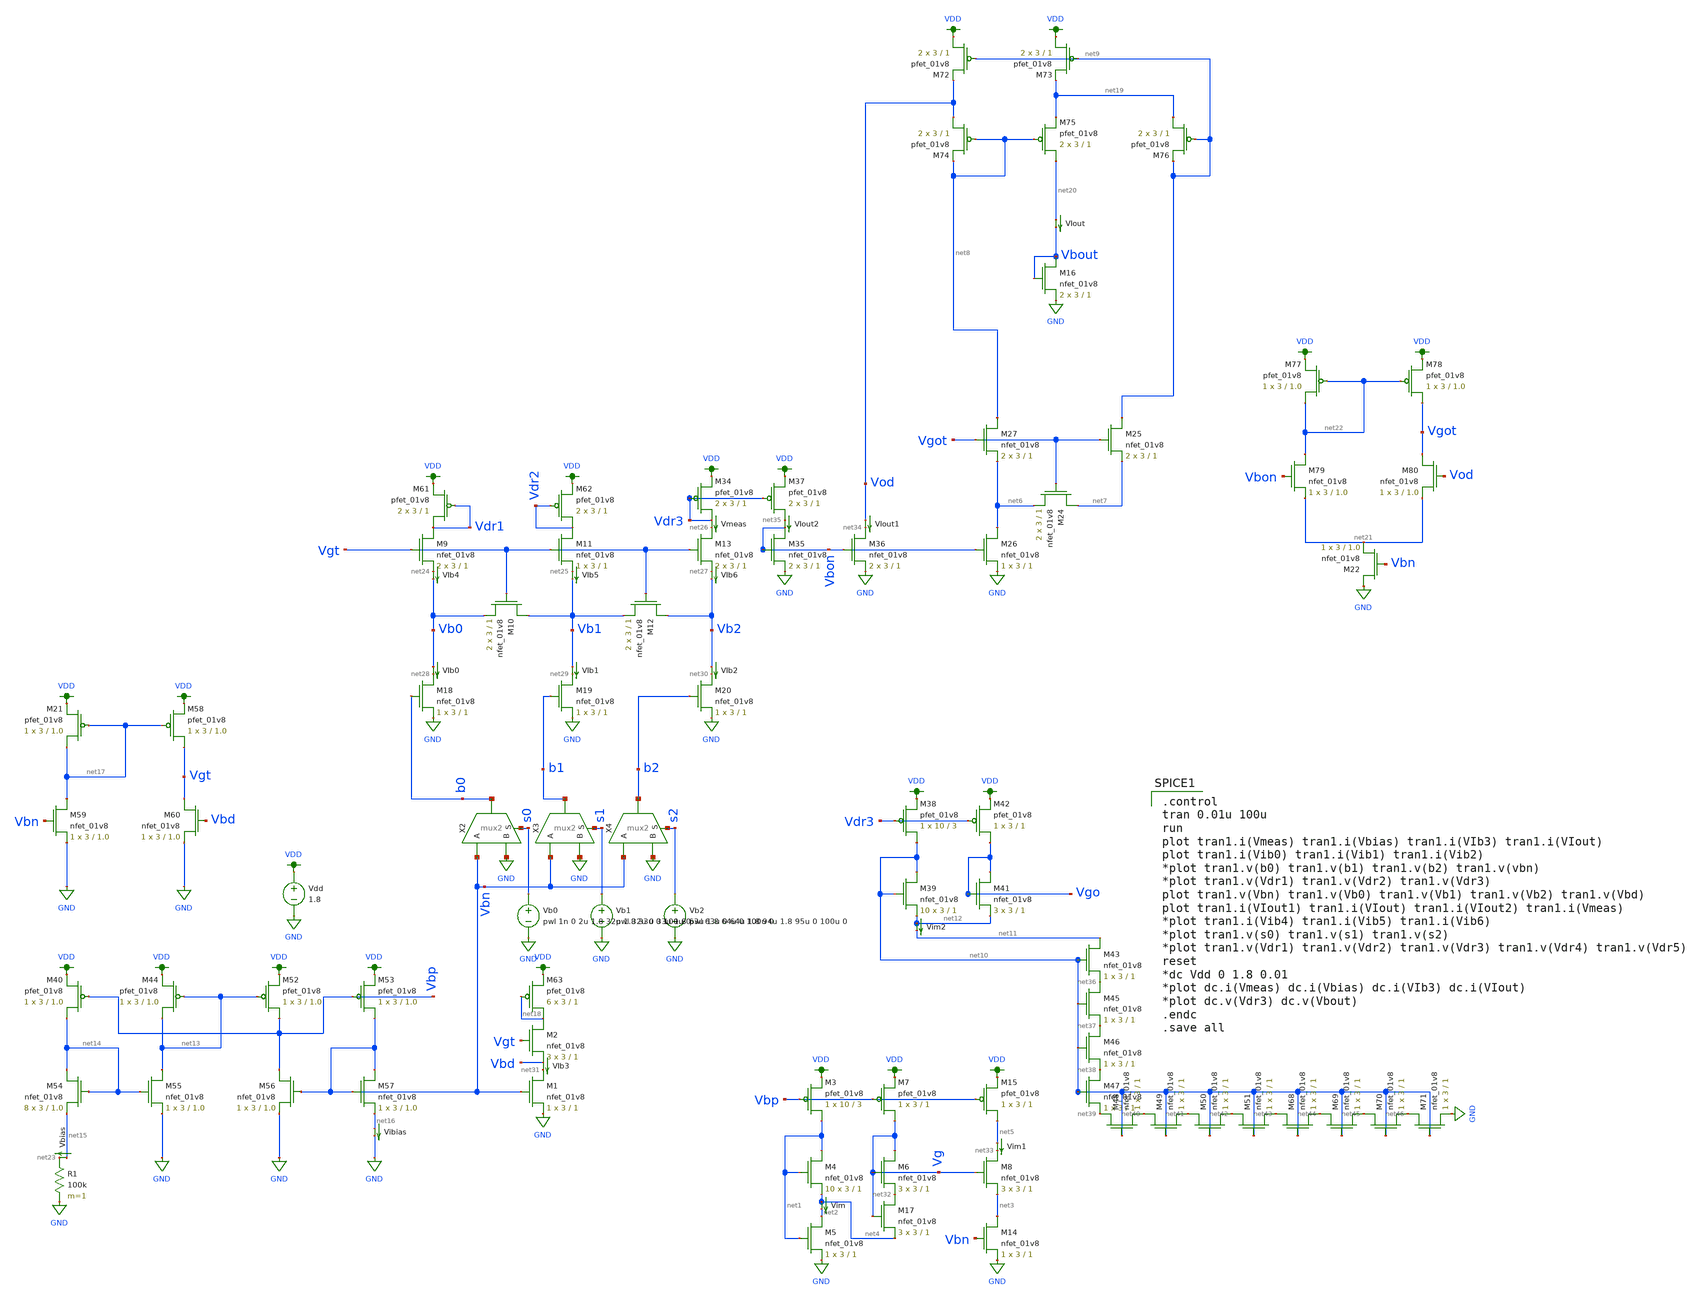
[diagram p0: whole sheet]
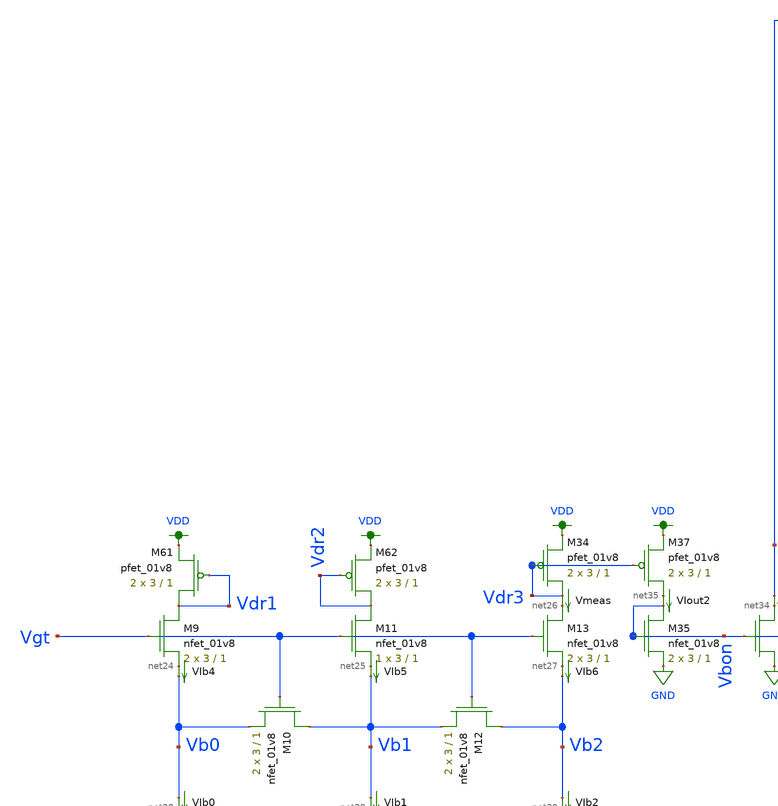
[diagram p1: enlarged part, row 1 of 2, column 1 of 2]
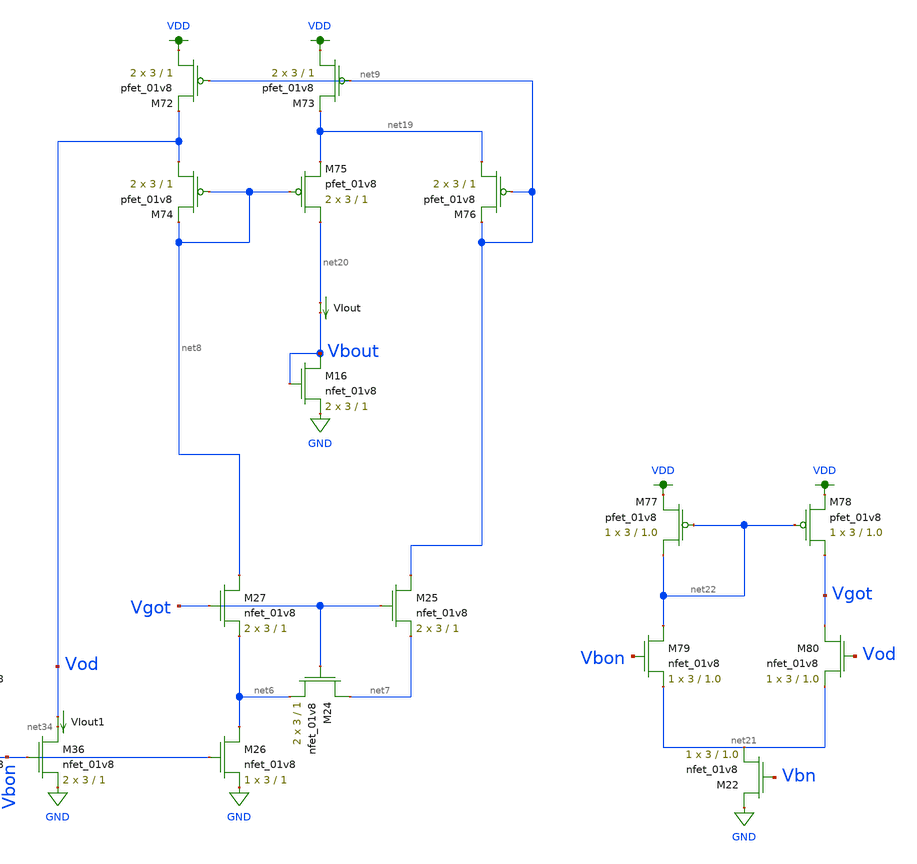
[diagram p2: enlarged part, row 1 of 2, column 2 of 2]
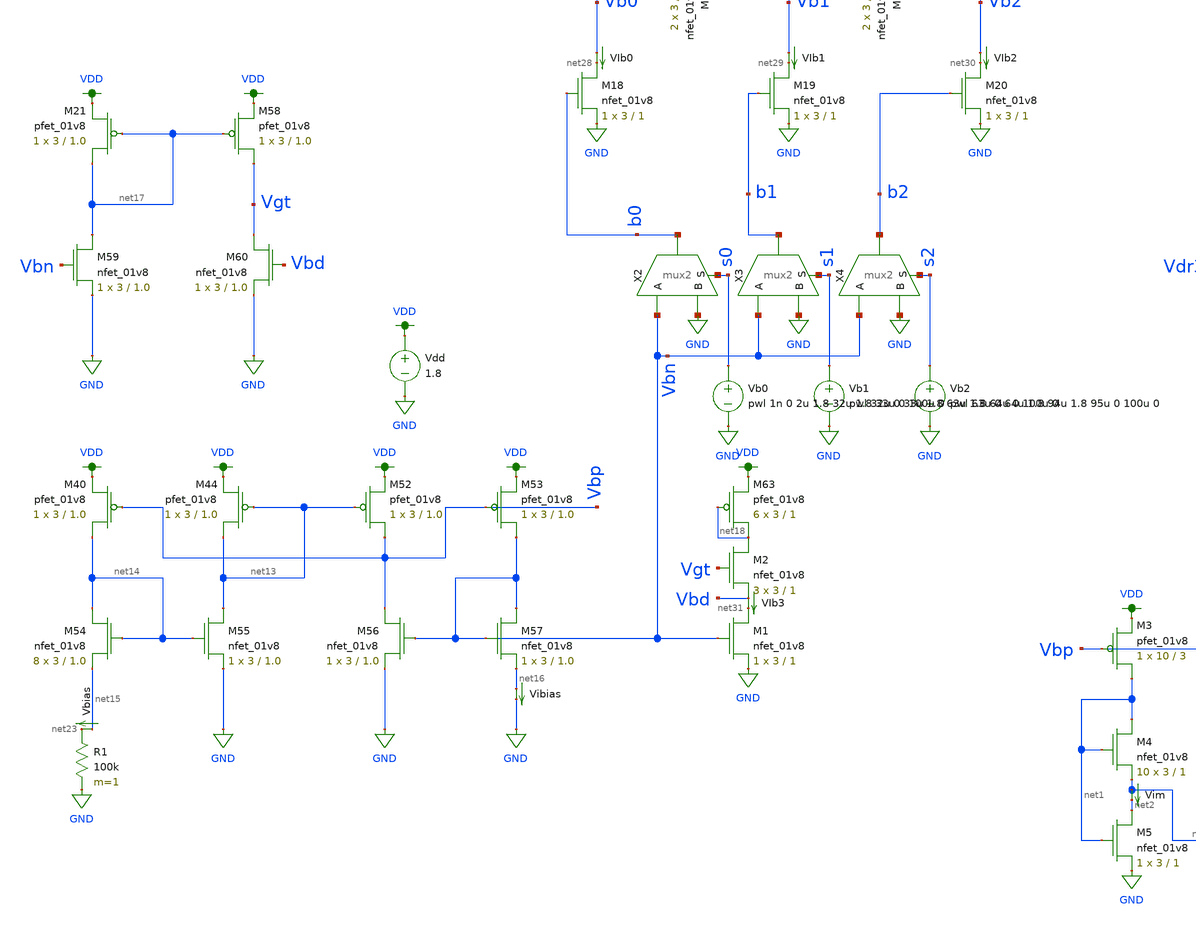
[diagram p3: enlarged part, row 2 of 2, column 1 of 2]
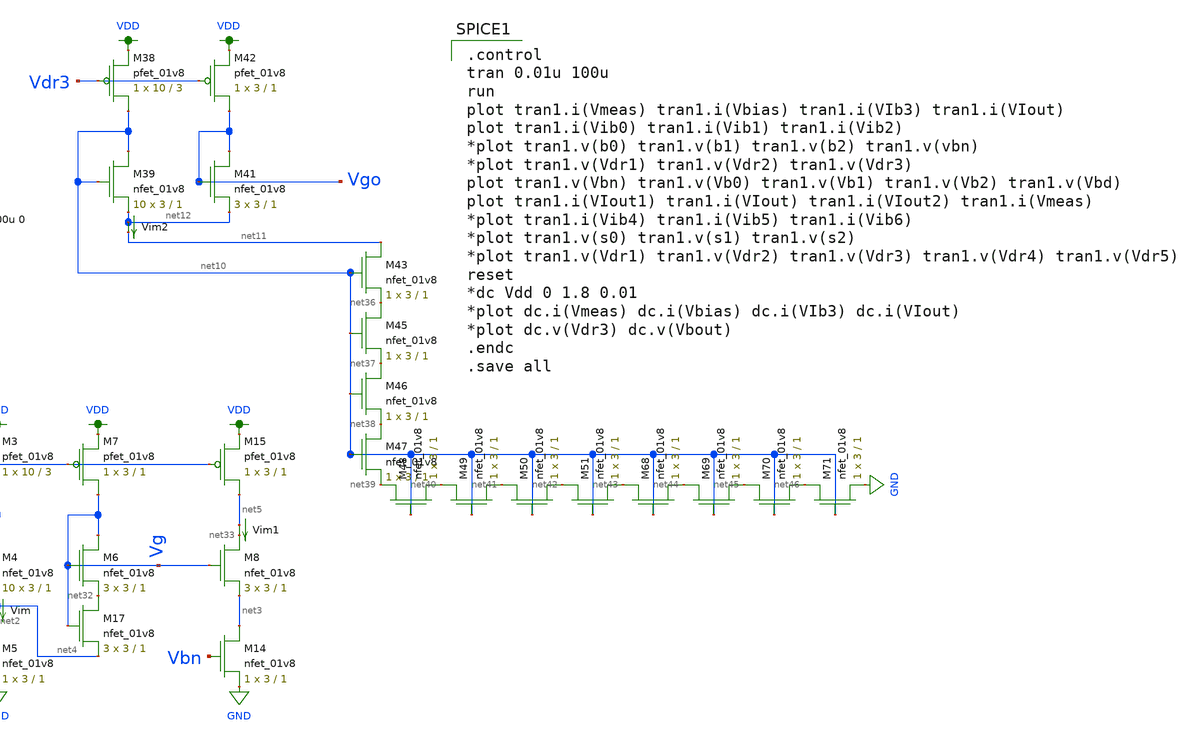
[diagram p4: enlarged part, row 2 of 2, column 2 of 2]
** sch_path: schematic/ladder3_test_josh_wilson_dynamic.sch
**.subckt ladder3_test_josh_wilson_dynamic
X2 b0 Vbn GND s0 mux2
X3 b1 Vbn GND s1 mux2
X4 b2 Vbn GND s2 mux2
R1 net23 GND 100k m=1
Vdd VDD GND 1.8
Vb0 s0 GND pwl 1n 0 2u 1.8 32u 1.8 33u 0 100u 0
Vb1 s1 GND pwl 32u 0 33u 1.8 63u 1.8 64u 0 100u 0
Vb2 s2 GND pwl 63u 0 64u 1.8 94u 1.8 95u 0 100u 0
XM9 Vdr1 Vgt net24 GND sky130_fd_pr__nfet_01v8 L=1 W=3 nf=1 ad='int((nf+1)/2) * W/nf * 0.29' as='int((nf+2)/2) * W/nf * 0.29'
+ pd='2*int((nf+1)/2) * (W/nf + 0.29)' ps='2*int((nf+2)/2) * (W/nf + 0.29)' nrd='0.29 / W' nrs='0.29 / W'
+ sa=0 sb=0 sd=0 mult=2 m=2
XM10 Vb1 Vgt Vb0 GND sky130_fd_pr__nfet_01v8 L=1 W=3 nf=1 ad='int((nf+1)/2) * W/nf * 0.29' as='int((nf+2)/2) * W/nf * 0.29'
+ pd='2*int((nf+1)/2) * (W/nf + 0.29)' ps='2*int((nf+2)/2) * (W/nf + 0.29)' nrd='0.29 / W' nrs='0.29 / W'
+ sa=0 sb=0 sd=0 mult=2 m=2
XM11 Vdr2 Vgt net25 GND sky130_fd_pr__nfet_01v8 L=1 W=3 nf=1 ad='int((nf+1)/2) * W/nf * 0.29' as='int((nf+2)/2) * W/nf * 0.29'
+ pd='2*int((nf+1)/2) * (W/nf + 0.29)' ps='2*int((nf+2)/2) * (W/nf + 0.29)' nrd='0.29 / W' nrs='0.29 / W'
+ sa=0 sb=0 sd=0 mult=1 m=1
XM12 Vb2 Vgt Vb1 GND sky130_fd_pr__nfet_01v8 L=1 W=3 nf=1 ad='int((nf+1)/2) * W/nf * 0.29' as='int((nf+2)/2) * W/nf * 0.29'
+ pd='2*int((nf+1)/2) * (W/nf + 0.29)' ps='2*int((nf+2)/2) * (W/nf + 0.29)' nrd='0.29 / W' nrs='0.29 / W'
+ sa=0 sb=0 sd=0 mult=2 m=2
XM13 net26 Vgt net27 GND sky130_fd_pr__nfet_01v8 L=1 W=3 nf=1 ad='int((nf+1)/2) * W/nf * 0.29' as='int((nf+2)/2) * W/nf * 0.29'
+ pd='2*int((nf+1)/2) * (W/nf + 0.29)' ps='2*int((nf+2)/2) * (W/nf + 0.29)' nrd='0.29 / W' nrs='0.29 / W'
+ sa=0 sb=0 sd=0 mult=2 m=2
XM18 net28 b0 GND GND sky130_fd_pr__nfet_01v8 L=1 W=3 nf=1 ad='int((nf+1)/2) * W/nf * 0.29' as='int((nf+2)/2) * W/nf * 0.29'
+ pd='2*int((nf+1)/2) * (W/nf + 0.29)' ps='2*int((nf+2)/2) * (W/nf + 0.29)' nrd='0.29 / W' nrs='0.29 / W'
+ sa=0 sb=0 sd=0 mult=1 m=1
XM19 net29 b1 GND GND sky130_fd_pr__nfet_01v8 L=1 W=3 nf=1 ad='int((nf+1)/2) * W/nf * 0.29' as='int((nf+2)/2) * W/nf * 0.29'
+ pd='2*int((nf+1)/2) * (W/nf + 0.29)' ps='2*int((nf+2)/2) * (W/nf + 0.29)' nrd='0.29 / W' nrs='0.29 / W'
+ sa=0 sb=0 sd=0 mult=1 m=1
XM20 net30 b2 GND GND sky130_fd_pr__nfet_01v8 L=1 W=3 nf=1 ad='int((nf+1)/2) * W/nf * 0.29' as='int((nf+2)/2) * W/nf * 0.29'
+ pd='2*int((nf+1)/2) * (W/nf + 0.29)' ps='2*int((nf+2)/2) * (W/nf + 0.29)' nrd='0.29 / W' nrs='0.29 / W'
+ sa=0 sb=0 sd=0 mult=1 m=1
Vmeas Vdr3 net26 0
.save i(vmeas)
Vbias net15 net23 0
.save i(vbias)
VIb0 Vb0 net28 0
.save i(vib0)
VIb1 Vb1 net29 0
.save i(vib1)
VIb2 Vb2 net30 0
.save i(vib2)
XM1 net31 Vbn GND GND sky130_fd_pr__nfet_01v8 L=1 W=3 nf=1 ad='int((nf+1)/2) * W/nf * 0.29' as='int((nf+2)/2) * W/nf * 0.29'
+ pd='2*int((nf+1)/2) * (W/nf + 0.29)' ps='2*int((nf+2)/2) * (W/nf + 0.29)' nrd='0.29 / W' nrs='0.29 / W'
+ sa=0 sb=0 sd=0 mult=1 m=1
VIb3 Vbd net31 0
.save i(vib3)
XM3 net1 Vbp VDD VDD sky130_fd_pr__pfet_01v8 L=3 W=10 nf=1 ad='int((nf+1)/2) * W/nf * 0.29' as='int((nf+2)/2) * W/nf * 0.29'
+ pd='2*int((nf+1)/2) * (W/nf + 0.29)' ps='2*int((nf+2)/2) * (W/nf + 0.29)' nrd='0.29 / W' nrs='0.29 / W'
+ sa=0 sb=0 sd=0 mult=1 m=1
XM4 net1 net1 net4 GND sky130_fd_pr__nfet_01v8 L=1 W=3 nf=1 ad='int((nf+1)/2) * W/nf * 0.29' as='int((nf+2)/2) * W/nf * 0.29'
+ pd='2*int((nf+1)/2) * (W/nf + 0.29)' ps='2*int((nf+2)/2) * (W/nf + 0.29)' nrd='0.29 / W' nrs='0.29 / W'
+ sa=0 sb=0 sd=0 mult=10 m=10
XM5 net2 net1 GND GND sky130_fd_pr__nfet_01v8 L=1 W=3 nf=1 ad='int((nf+1)/2) * W/nf * 0.29' as='int((nf+2)/2) * W/nf * 0.29'
+ pd='2*int((nf+1)/2) * (W/nf + 0.29)' ps='2*int((nf+2)/2) * (W/nf + 0.29)' nrd='0.29 / W' nrs='0.29 / W'
+ sa=0 sb=0 sd=0 mult=1 m=1
Vim net4 net2 0
.save i(vim)
XM6 Vg Vg net32 GND sky130_fd_pr__nfet_01v8 L=1 W=3 nf=1 ad='int((nf+1)/2) * W/nf * 0.29' as='int((nf+2)/2) * W/nf * 0.29'
+ pd='2*int((nf+1)/2) * (W/nf + 0.29)' ps='2*int((nf+2)/2) * (W/nf + 0.29)' nrd='0.29 / W' nrs='0.29 / W'
+ sa=0 sb=0 sd=0 mult=3 m=3
XM7 Vg Vbp VDD VDD sky130_fd_pr__pfet_01v8 L=1 W=3 nf=1 ad='int((nf+1)/2) * W/nf * 0.29' as='int((nf+2)/2) * W/nf * 0.29'
+ pd='2*int((nf+1)/2) * (W/nf + 0.29)' ps='2*int((nf+2)/2) * (W/nf + 0.29)' nrd='0.29 / W' nrs='0.29 / W'
+ sa=0 sb=0 sd=0 mult=1 m=1
XM8 net33 Vg net3 GND sky130_fd_pr__nfet_01v8 L=1 W=3 nf=1 ad='int((nf+1)/2) * W/nf * 0.29' as='int((nf+2)/2) * W/nf * 0.29'
+ pd='2*int((nf+1)/2) * (W/nf + 0.29)' ps='2*int((nf+2)/2) * (W/nf + 0.29)' nrd='0.29 / W' nrs='0.29 / W'
+ sa=0 sb=0 sd=0 mult=3 m=3
XM14 net3 Vbn GND GND sky130_fd_pr__nfet_01v8 L=1 W=3 nf=1 ad='int((nf+1)/2) * W/nf * 0.29' as='int((nf+2)/2) * W/nf * 0.29'
+ pd='2*int((nf+1)/2) * (W/nf + 0.29)' ps='2*int((nf+2)/2) * (W/nf + 0.29)' nrd='0.29 / W' nrs='0.29 / W'
+ sa=0 sb=0 sd=0 mult=1 m=1
Vim1 net5 net33 0
.save i(vim1)
XM15 net5 Vbp VDD VDD sky130_fd_pr__pfet_01v8 L=1 W=3 nf=1 ad='int((nf+1)/2) * W/nf * 0.29' as='int((nf+2)/2) * W/nf * 0.29'
+ pd='2*int((nf+1)/2) * (W/nf + 0.29)' ps='2*int((nf+2)/2) * (W/nf + 0.29)' nrd='0.29 / W' nrs='0.29 / W'
+ sa=0 sb=0 sd=0 mult=1 m=1
VIb4 net24 Vb0 0
.save i(vib4)
VIb5 net25 Vb1 0
.save i(vib5)
VIb6 net27 Vb2 0
.save i(vib6)
VIout net20 Vbout 0
.save i(viout)
XM24 net7 Vgot net6 GND sky130_fd_pr__nfet_01v8 L=1 W=3 nf=1 ad='int((nf+1)/2) * W/nf * 0.29' as='int((nf+2)/2) * W/nf * 0.29'
+ pd='2*int((nf+1)/2) * (W/nf + 0.29)' ps='2*int((nf+2)/2) * (W/nf + 0.29)' nrd='0.29 / W' nrs='0.29 / W'
+ sa=0 sb=0 sd=0 mult=2 m=2
XM25 net9 Vgot net7 GND sky130_fd_pr__nfet_01v8 L=1 W=3 nf=1 ad='int((nf+1)/2) * W/nf * 0.29' as='int((nf+2)/2) * W/nf * 0.29'
+ pd='2*int((nf+1)/2) * (W/nf + 0.29)' ps='2*int((nf+2)/2) * (W/nf + 0.29)' nrd='0.29 / W' nrs='0.29 / W'
+ sa=0 sb=0 sd=0 mult=2 m=2
XM26 net6 Vbon GND GND sky130_fd_pr__nfet_01v8 L=1 W=3 nf=1 ad='int((nf+1)/2) * W/nf * 0.29' as='int((nf+2)/2) * W/nf * 0.29'
+ pd='2*int((nf+1)/2) * (W/nf + 0.29)' ps='2*int((nf+2)/2) * (W/nf + 0.29)' nrd='0.29 / W' nrs='0.29 / W'
+ sa=0 sb=0 sd=0 mult=1 m=1
XM27 net8 Vgot net6 GND sky130_fd_pr__nfet_01v8 L=1 W=3 nf=1 ad='int((nf+1)/2) * W/nf * 0.29' as='int((nf+2)/2) * W/nf * 0.29'
+ pd='2*int((nf+1)/2) * (W/nf + 0.29)' ps='2*int((nf+2)/2) * (W/nf + 0.29)' nrd='0.29 / W' nrs='0.29 / W'
+ sa=0 sb=0 sd=0 mult=2 m=2
XM16 Vbout Vbout GND GND sky130_fd_pr__nfet_01v8 L=1 W=3 nf=1 ad='int((nf+1)/2) * W/nf * 0.29' as='int((nf+2)/2) * W/nf * 0.29'
+ pd='2*int((nf+1)/2) * (W/nf + 0.29)' ps='2*int((nf+2)/2) * (W/nf + 0.29)' nrd='0.29 / W' nrs='0.29 / W'
+ sa=0 sb=0 sd=0 mult=2 m=2
XM34 Vdr3 Vdr3 VDD VDD sky130_fd_pr__pfet_01v8 L=1 W=3 nf=1 ad='int((nf+1)/2) * W/nf * 0.29' as='int((nf+2)/2) * W/nf * 0.29'
+ pd='2*int((nf+1)/2) * (W/nf + 0.29)' ps='2*int((nf+2)/2) * (W/nf + 0.29)' nrd='0.29 / W' nrs='0.29 / W'
+ sa=0 sb=0 sd=0 mult=2 m=2
XM35 Vbon Vbon GND GND sky130_fd_pr__nfet_01v8 L=1 W=3 nf=1 ad='int((nf+1)/2) * W/nf * 0.29' as='int((nf+2)/2) * W/nf * 0.29'
+ pd='2*int((nf+1)/2) * (W/nf + 0.29)' ps='2*int((nf+2)/2) * (W/nf + 0.29)' nrd='0.29 / W' nrs='0.29 / W'
+ sa=0 sb=0 sd=0 mult=2 m=2
XM36 net34 Vbon GND GND sky130_fd_pr__nfet_01v8 L=1 W=3 nf=1 ad='int((nf+1)/2) * W/nf * 0.29' as='int((nf+2)/2) * W/nf * 0.29'
+ pd='2*int((nf+1)/2) * (W/nf + 0.29)' ps='2*int((nf+2)/2) * (W/nf + 0.29)' nrd='0.29 / W' nrs='0.29 / W'
+ sa=0 sb=0 sd=0 mult=2 m=2
XM37 net35 Vdr3 VDD VDD sky130_fd_pr__pfet_01v8 L=1 W=3 nf=1 ad='int((nf+1)/2) * W/nf * 0.29' as='int((nf+2)/2) * W/nf * 0.29'
+ pd='2*int((nf+1)/2) * (W/nf + 0.29)' ps='2*int((nf+2)/2) * (W/nf + 0.29)' nrd='0.29 / W' nrs='0.29 / W'
+ sa=0 sb=0 sd=0 mult=2 m=2
XM38 net10 Vdr3 VDD VDD sky130_fd_pr__pfet_01v8 L=3 W=10 nf=1 ad='int((nf+1)/2) * W/nf * 0.29' as='int((nf+2)/2) * W/nf * 0.29'
+ pd='2*int((nf+1)/2) * (W/nf + 0.29)' ps='2*int((nf+2)/2) * (W/nf + 0.29)' nrd='0.29 / W' nrs='0.29 / W'
+ sa=0 sb=0 sd=0 mult=1 m=1
XM39 net10 net10 net12 GND sky130_fd_pr__nfet_01v8 L=1 W=3 nf=1 ad='int((nf+1)/2) * W/nf * 0.29' as='int((nf+2)/2) * W/nf * 0.29'
+ pd='2*int((nf+1)/2) * (W/nf + 0.29)' ps='2*int((nf+2)/2) * (W/nf + 0.29)' nrd='0.29 / W' nrs='0.29 / W'
+ sa=0 sb=0 sd=0 mult=10 m=10
Vim2 net12 net11 0
.save i(vim2)
XM41 Vgo Vgo net12 GND sky130_fd_pr__nfet_01v8 L=1 W=3 nf=1 ad='int((nf+1)/2) * W/nf * 0.29' as='int((nf+2)/2) * W/nf * 0.29'
+ pd='2*int((nf+1)/2) * (W/nf + 0.29)' ps='2*int((nf+2)/2) * (W/nf + 0.29)' nrd='0.29 / W' nrs='0.29 / W'
+ sa=0 sb=0 sd=0 mult=3 m=3
XM42 Vgo Vdr3 VDD VDD sky130_fd_pr__pfet_01v8 L=1 W=3 nf=1 ad='int((nf+1)/2) * W/nf * 0.29' as='int((nf+2)/2) * W/nf * 0.29'
+ pd='2*int((nf+1)/2) * (W/nf + 0.29)' ps='2*int((nf+2)/2) * (W/nf + 0.29)' nrd='0.29 / W' nrs='0.29 / W'
+ sa=0 sb=0 sd=0 mult=1 m=1
XM43 net11 net10 net36 GND sky130_fd_pr__nfet_01v8 L=1 W=3 nf=1 ad='int((nf+1)/2) * W/nf * 0.29' as='int((nf+2)/2) * W/nf * 0.29'
+ pd='2*int((nf+1)/2) * (W/nf + 0.29)' ps='2*int((nf+2)/2) * (W/nf + 0.29)' nrd='0.29 / W' nrs='0.29 / W'
+ sa=0 sb=0 sd=0 mult=1 m=1
XM45 net36 net10 net37 GND sky130_fd_pr__nfet_01v8 L=1 W=3 nf=1 ad='int((nf+1)/2) * W/nf * 0.29' as='int((nf+2)/2) * W/nf * 0.29'
+ pd='2*int((nf+1)/2) * (W/nf + 0.29)' ps='2*int((nf+2)/2) * (W/nf + 0.29)' nrd='0.29 / W' nrs='0.29 / W'
+ sa=0 sb=0 sd=0 mult=1 m=1
XM46 net37 net10 net38 GND sky130_fd_pr__nfet_01v8 L=1 W=3 nf=1 ad='int((nf+1)/2) * W/nf * 0.29' as='int((nf+2)/2) * W/nf * 0.29'
+ pd='2*int((nf+1)/2) * (W/nf + 0.29)' ps='2*int((nf+2)/2) * (W/nf + 0.29)' nrd='0.29 / W' nrs='0.29 / W'
+ sa=0 sb=0 sd=0 mult=1 m=1
XM47 net38 net10 net39 GND sky130_fd_pr__nfet_01v8 L=1 W=3 nf=1 ad='int((nf+1)/2) * W/nf * 0.29' as='int((nf+2)/2) * W/nf * 0.29'
+ pd='2*int((nf+1)/2) * (W/nf + 0.29)' ps='2*int((nf+2)/2) * (W/nf + 0.29)' nrd='0.29 / W' nrs='0.29 / W'
+ sa=0 sb=0 sd=0 mult=1 m=1
XM48 net39 net10 net40 GND sky130_fd_pr__nfet_01v8 L=1 W=3 nf=1 ad='int((nf+1)/2) * W/nf * 0.29' as='int((nf+2)/2) * W/nf * 0.29'
+ pd='2*int((nf+1)/2) * (W/nf + 0.29)' ps='2*int((nf+2)/2) * (W/nf + 0.29)' nrd='0.29 / W' nrs='0.29 / W'
+ sa=0 sb=0 sd=0 mult=1 m=1
XM49 net40 net10 net41 GND sky130_fd_pr__nfet_01v8 L=1 W=3 nf=1 ad='int((nf+1)/2) * W/nf * 0.29' as='int((nf+2)/2) * W/nf * 0.29'
+ pd='2*int((nf+1)/2) * (W/nf + 0.29)' ps='2*int((nf+2)/2) * (W/nf + 0.29)' nrd='0.29 / W' nrs='0.29 / W'
+ sa=0 sb=0 sd=0 mult=1 m=1
XM50 net41 net10 net42 GND sky130_fd_pr__nfet_01v8 L=1 W=3 nf=1 ad='int((nf+1)/2) * W/nf * 0.29' as='int((nf+2)/2) * W/nf * 0.29'
+ pd='2*int((nf+1)/2) * (W/nf + 0.29)' ps='2*int((nf+2)/2) * (W/nf + 0.29)' nrd='0.29 / W' nrs='0.29 / W'
+ sa=0 sb=0 sd=0 mult=1 m=1
XM51 net42 net10 net43 GND sky130_fd_pr__nfet_01v8 L=1 W=3 nf=1 ad='int((nf+1)/2) * W/nf * 0.29' as='int((nf+2)/2) * W/nf * 0.29'
+ pd='2*int((nf+1)/2) * (W/nf + 0.29)' ps='2*int((nf+2)/2) * (W/nf + 0.29)' nrd='0.29 / W' nrs='0.29 / W'
+ sa=0 sb=0 sd=0 mult=1 m=1
XM40 net14 Vbp VDD VDD sky130_fd_pr__pfet_01v8 L=1.0 W=3 nf=1 ad='int((nf+1)/2) * W/nf * 0.29' as='int((nf+2)/2) * W/nf * 0.29'
+ pd='2*int((nf+1)/2) * (W/nf + 0.29)' ps='2*int((nf+2)/2) * (W/nf + 0.29)' nrd='0.29 / W' nrs='0.29 / W'
+ sa=0 sb=0 sd=0 mult=1 m=1
XM44 net13 net13 VDD VDD sky130_fd_pr__pfet_01v8 L=1.0 W=3 nf=1 ad='int((nf+1)/2) * W/nf * 0.29' as='int((nf+2)/2) * W/nf * 0.29'
+ pd='2*int((nf+1)/2) * (W/nf + 0.29)' ps='2*int((nf+2)/2) * (W/nf + 0.29)' nrd='0.29 / W' nrs='0.29 / W'
+ sa=0 sb=0 sd=0 mult=1 m=1
XM52 Vbp net13 VDD VDD sky130_fd_pr__pfet_01v8 L=1.0 W=3 nf=1 ad='int((nf+1)/2) * W/nf * 0.29' as='int((nf+2)/2) * W/nf * 0.29'
+ pd='2*int((nf+1)/2) * (W/nf + 0.29)' ps='2*int((nf+2)/2) * (W/nf + 0.29)' nrd='0.29 / W' nrs='0.29 / W'
+ sa=0 sb=0 sd=0 mult=1 m=1
XM53 Vbn Vbp VDD VDD sky130_fd_pr__pfet_01v8 L=1.0 W=3 nf=1 ad='int((nf+1)/2) * W/nf * 0.29' as='int((nf+2)/2) * W/nf * 0.29'
+ pd='2*int((nf+1)/2) * (W/nf + 0.29)' ps='2*int((nf+2)/2) * (W/nf + 0.29)' nrd='0.29 / W' nrs='0.29 / W'
+ sa=0 sb=0 sd=0 mult=1 m=1
XM54 net14 net14 net15 GND sky130_fd_pr__nfet_01v8 L=1.0 W=3 nf=1 ad='int((nf+1)/2) * W/nf * 0.29' as='int((nf+2)/2) * W/nf * 0.29'
+ pd='2*int((nf+1)/2) * (W/nf + 0.29)' ps='2*int((nf+2)/2) * (W/nf + 0.29)' nrd='0.29 / W' nrs='0.29 / W'
+ sa=0 sb=0 sd=0 mult=8 m=8
XM55 net13 net14 GND GND sky130_fd_pr__nfet_01v8 L=1.0 W=3 nf=1 ad='int((nf+1)/2) * W/nf * 0.29' as='int((nf+2)/2) * W/nf * 0.29'
+ pd='2*int((nf+1)/2) * (W/nf + 0.29)' ps='2*int((nf+2)/2) * (W/nf + 0.29)' nrd='0.29 / W' nrs='0.29 / W'
+ sa=0 sb=0 sd=0 mult=1 m=1
XM56 Vbp Vbn GND GND sky130_fd_pr__nfet_01v8 L=1.0 W=3 nf=1 ad='int((nf+1)/2) * W/nf * 0.29' as='int((nf+2)/2) * W/nf * 0.29'
+ pd='2*int((nf+1)/2) * (W/nf + 0.29)' ps='2*int((nf+2)/2) * (W/nf + 0.29)' nrd='0.29 / W' nrs='0.29 / W'
+ sa=0 sb=0 sd=0 mult=1 m=1
XM57 Vbn Vbn net16 GND sky130_fd_pr__nfet_01v8 L=1.0 W=3 nf=1 ad='int((nf+1)/2) * W/nf * 0.29' as='int((nf+2)/2) * W/nf * 0.29'
+ pd='2*int((nf+1)/2) * (W/nf + 0.29)' ps='2*int((nf+2)/2) * (W/nf + 0.29)' nrd='0.29 / W' nrs='0.29 / W'
+ sa=0 sb=0 sd=0 mult=1 m=1
Vibias net16 GND 0
.save i(vibias)
XM2 net18 Vgt Vbd GND sky130_fd_pr__nfet_01v8 L=1 W=3 nf=1 ad='int((nf+1)/2) * W/nf * 0.29' as='int((nf+2)/2) * W/nf * 0.29'
+ pd='2*int((nf+1)/2) * (W/nf + 0.29)' ps='2*int((nf+2)/2) * (W/nf + 0.29)' nrd='0.29 / W' nrs='0.29 / W'
+ sa=0 sb=0 sd=0 mult=3 m=3
XM17 net32 Vg net4 GND sky130_fd_pr__nfet_01v8 L=1 W=3 nf=1 ad='int((nf+1)/2) * W/nf * 0.29' as='int((nf+2)/2) * W/nf * 0.29'
+ pd='2*int((nf+1)/2) * (W/nf + 0.29)' ps='2*int((nf+2)/2) * (W/nf + 0.29)' nrd='0.29 / W' nrs='0.29 / W'
+ sa=0 sb=0 sd=0 mult=3 m=3
XM21 net17 net17 VDD VDD sky130_fd_pr__pfet_01v8 L=1.0 W=3 nf=1 ad='int((nf+1)/2) * W/nf * 0.29' as='int((nf+2)/2) * W/nf * 0.29'
+ pd='2*int((nf+1)/2) * (W/nf + 0.29)' ps='2*int((nf+2)/2) * (W/nf + 0.29)' nrd='0.29 / W' nrs='0.29 / W'
+ sa=0 sb=0 sd=0 mult=1 m=1
XM58 Vgt net17 VDD VDD sky130_fd_pr__pfet_01v8 L=1.0 W=3 nf=1 ad='int((nf+1)/2) * W/nf * 0.29' as='int((nf+2)/2) * W/nf * 0.29'
+ pd='2*int((nf+1)/2) * (W/nf + 0.29)' ps='2*int((nf+2)/2) * (W/nf + 0.29)' nrd='0.29 / W' nrs='0.29 / W'
+ sa=0 sb=0 sd=0 mult=1 m=1
XM59 net17 Vbn GND GND sky130_fd_pr__nfet_01v8 L=1.0 W=3 nf=1 ad='int((nf+1)/2) * W/nf * 0.29' as='int((nf+2)/2) * W/nf * 0.29'
+ pd='2*int((nf+1)/2) * (W/nf + 0.29)' ps='2*int((nf+2)/2) * (W/nf + 0.29)' nrd='0.29 / W' nrs='0.29 / W'
+ sa=0 sb=0 sd=0 mult=1 m=1
XM60 Vgt Vbd GND GND sky130_fd_pr__nfet_01v8 L=1.0 W=3 nf=1 ad='int((nf+1)/2) * W/nf * 0.29' as='int((nf+2)/2) * W/nf * 0.29'
+ pd='2*int((nf+1)/2) * (W/nf + 0.29)' ps='2*int((nf+2)/2) * (W/nf + 0.29)' nrd='0.29 / W' nrs='0.29 / W'
+ sa=0 sb=0 sd=0 mult=1 m=1
XM61 Vdr1 Vdr1 VDD VDD sky130_fd_pr__pfet_01v8 L=1 W=3 nf=1 ad='int((nf+1)/2) * W/nf * 0.29' as='int((nf+2)/2) * W/nf * 0.29'
+ pd='2*int((nf+1)/2) * (W/nf + 0.29)' ps='2*int((nf+2)/2) * (W/nf + 0.29)' nrd='0.29 / W' nrs='0.29 / W'
+ sa=0 sb=0 sd=0 mult=2 m=2
XM62 Vdr2 Vdr2 VDD VDD sky130_fd_pr__pfet_01v8 L=1 W=3 nf=1 ad='int((nf+1)/2) * W/nf * 0.29' as='int((nf+2)/2) * W/nf * 0.29'
+ pd='2*int((nf+1)/2) * (W/nf + 0.29)' ps='2*int((nf+2)/2) * (W/nf + 0.29)' nrd='0.29 / W' nrs='0.29 / W'
+ sa=0 sb=0 sd=0 mult=2 m=2
XM63 net18 net18 VDD VDD sky130_fd_pr__pfet_01v8 L=1 W=3 nf=1 ad='int((nf+1)/2) * W/nf * 0.29' as='int((nf+2)/2) * W/nf * 0.29'
+ pd='2*int((nf+1)/2) * (W/nf + 0.29)' ps='2*int((nf+2)/2) * (W/nf + 0.29)' nrd='0.29 / W' nrs='0.29 / W'
+ sa=0 sb=0 sd=0 mult=6 m=6
XM68 net43 net10 net44 GND sky130_fd_pr__nfet_01v8 L=1 W=3 nf=1 ad='int((nf+1)/2) * W/nf * 0.29' as='int((nf+2)/2) * W/nf * 0.29'
+ pd='2*int((nf+1)/2) * (W/nf + 0.29)' ps='2*int((nf+2)/2) * (W/nf + 0.29)' nrd='0.29 / W' nrs='0.29 / W'
+ sa=0 sb=0 sd=0 mult=1 m=1
XM69 net44 net10 net45 GND sky130_fd_pr__nfet_01v8 L=1 W=3 nf=1 ad='int((nf+1)/2) * W/nf * 0.29' as='int((nf+2)/2) * W/nf * 0.29'
+ pd='2*int((nf+1)/2) * (W/nf + 0.29)' ps='2*int((nf+2)/2) * (W/nf + 0.29)' nrd='0.29 / W' nrs='0.29 / W'
+ sa=0 sb=0 sd=0 mult=1 m=1
XM70 net45 net10 net46 GND sky130_fd_pr__nfet_01v8 L=1 W=3 nf=1 ad='int((nf+1)/2) * W/nf * 0.29' as='int((nf+2)/2) * W/nf * 0.29'
+ pd='2*int((nf+1)/2) * (W/nf + 0.29)' ps='2*int((nf+2)/2) * (W/nf + 0.29)' nrd='0.29 / W' nrs='0.29 / W'
+ sa=0 sb=0 sd=0 mult=1 m=1
XM71 net46 net10 GND GND sky130_fd_pr__nfet_01v8 L=1 W=3 nf=1 ad='int((nf+1)/2) * W/nf * 0.29' as='int((nf+2)/2) * W/nf * 0.29'
+ pd='2*int((nf+1)/2) * (W/nf + 0.29)' ps='2*int((nf+2)/2) * (W/nf + 0.29)' nrd='0.29 / W' nrs='0.29 / W'
+ sa=0 sb=0 sd=0 mult=1 m=1
VIout1 Vod net34 0
.save i(viout1)
VIout2 net35 Vbon 0
.save i(viout2)
XM72 VDD net9 Vod VDD sky130_fd_pr__pfet_01v8 L=1 W=3 nf=1 ad='int((nf+1)/2) * W/nf * 0.29' as='int((nf+2)/2) * W/nf * 0.29'
+ pd='2*int((nf+1)/2) * (W/nf + 0.29)' ps='2*int((nf+2)/2) * (W/nf + 0.29)' nrd='0.29 / W' nrs='0.29 / W'
+ sa=0 sb=0 sd=0 mult=2 m=2
XM73 VDD net9 net19 VDD sky130_fd_pr__pfet_01v8 L=1 W=3 nf=1 ad='int((nf+1)/2) * W/nf * 0.29' as='int((nf+2)/2) * W/nf * 0.29'
+ pd='2*int((nf+1)/2) * (W/nf + 0.29)' ps='2*int((nf+2)/2) * (W/nf + 0.29)' nrd='0.29 / W' nrs='0.29 / W'
+ sa=0 sb=0 sd=0 mult=2 m=2
XM74 Vod net8 net8 VDD sky130_fd_pr__pfet_01v8 L=1 W=3 nf=1 ad='int((nf+1)/2) * W/nf * 0.29' as='int((nf+2)/2) * W/nf * 0.29'
+ pd='2*int((nf+1)/2) * (W/nf + 0.29)' ps='2*int((nf+2)/2) * (W/nf + 0.29)' nrd='0.29 / W' nrs='0.29 / W'
+ sa=0 sb=0 sd=0 mult=2 m=2
XM75 net20 net8 net19 VDD sky130_fd_pr__pfet_01v8 L=1 W=3 nf=1 ad='int((nf+1)/2) * W/nf * 0.29' as='int((nf+2)/2) * W/nf * 0.29'
+ pd='2*int((nf+1)/2) * (W/nf + 0.29)' ps='2*int((nf+2)/2) * (W/nf + 0.29)' nrd='0.29 / W' nrs='0.29 / W'
+ sa=0 sb=0 sd=0 mult=2 m=2
XM76 net19 net9 net9 VDD sky130_fd_pr__pfet_01v8 L=1 W=3 nf=1 ad='int((nf+1)/2) * W/nf * 0.29' as='int((nf+2)/2) * W/nf * 0.29'
+ pd='2*int((nf+1)/2) * (W/nf + 0.29)' ps='2*int((nf+2)/2) * (W/nf + 0.29)' nrd='0.29 / W' nrs='0.29 / W'
+ sa=0 sb=0 sd=0 mult=2 m=2
XM77 net22 net22 VDD VDD sky130_fd_pr__pfet_01v8 L=1.0 W=3 nf=1 ad='int((nf+1)/2) * W/nf * 0.29' as='int((nf+2)/2) * W/nf * 0.29'
+ pd='2*int((nf+1)/2) * (W/nf + 0.29)' ps='2*int((nf+2)/2) * (W/nf + 0.29)' nrd='0.29 / W' nrs='0.29 / W'
+ sa=0 sb=0 sd=0 mult=1 m=1
XM78 Vgot net22 VDD VDD sky130_fd_pr__pfet_01v8 L=1.0 W=3 nf=1 ad='int((nf+1)/2) * W/nf * 0.29' as='int((nf+2)/2) * W/nf * 0.29'
+ pd='2*int((nf+1)/2) * (W/nf + 0.29)' ps='2*int((nf+2)/2) * (W/nf + 0.29)' nrd='0.29 / W' nrs='0.29 / W'
+ sa=0 sb=0 sd=0 mult=1 m=1
XM79 net22 Vbon net21 GND sky130_fd_pr__nfet_01v8 L=1.0 W=3 nf=1 ad='int((nf+1)/2) * W/nf * 0.29' as='int((nf+2)/2) * W/nf * 0.29'
+ pd='2*int((nf+1)/2) * (W/nf + 0.29)' ps='2*int((nf+2)/2) * (W/nf + 0.29)' nrd='0.29 / W' nrs='0.29 / W'
+ sa=0 sb=0 sd=0 mult=1 m=1
XM80 Vgot Vod net21 GND sky130_fd_pr__nfet_01v8 L=1.0 W=3 nf=1 ad='int((nf+1)/2) * W/nf * 0.29' as='int((nf+2)/2) * W/nf * 0.29'
+ pd='2*int((nf+1)/2) * (W/nf + 0.29)' ps='2*int((nf+2)/2) * (W/nf + 0.29)' nrd='0.29 / W' nrs='0.29 / W'
+ sa=0 sb=0 sd=0 mult=1 m=1
XM22 GND Vbn net21 GND sky130_fd_pr__nfet_01v8 L=1.0 W=3 nf=1 ad='int((nf+1)/2) * W/nf * 0.29' as='int((nf+2)/2) * W/nf * 0.29'
+ pd='2*int((nf+1)/2) * (W/nf + 0.29)' ps='2*int((nf+2)/2) * (W/nf + 0.29)' nrd='0.29 / W' nrs='0.29 / W'
+ sa=0 sb=0 sd=0 mult=1 m=1
**** begin user architecture code

.option wnflag=1
.param MC_SWITCH=0.0
.lib ~/skywater/skywater-pdk/libraries/sky130_fd_pr_ngspice/latest/models/sky130.lib.spice tt


.control
tran 0.01u 100u
run
plot tran1.i(Vmeas) tran1.i(Vbias) tran1.i(VIb3) tran1.i(VIout)
plot tran1.i(Vib0) tran1.i(Vib1) tran1.i(Vib2)
*plot tran1.v(b0) tran1.v(b1) tran1.v(b2) tran1.v(vbn)
*plot tran1.v(Vdr1) tran1.v(Vdr2) tran1.v(Vdr3)
plot tran1.v(Vbn) tran1.v(Vb0) tran1.v(Vb1) tran1.v(Vb2) tran1.v(Vbd)
plot tran1.i(VIout1) tran1.i(VIout) tran1.i(VIout2) tran1.i(Vmeas)
*plot tran1.i(Vib4) tran1.i(Vib5) tran1.i(Vib6)
*plot tran1.v(s0) tran1.v(s1) tran1.v(s2)
*plot tran1.v(Vdr1) tran1.v(Vdr2) tran1.v(Vdr3) tran1.v(Vdr4) tran1.v(Vdr5)
reset
*dc Vdd 0 1.8 0.01
*plot dc.i(Vmeas) dc.i(Vbias) dc.i(VIb3) dc.i(VIout)
*plot dc.v(Vdr3) dc.v(Vbout)
.endc
.save all

**** end user architecture code
**.ends
.GLOBAL GND
.GLOBAL VDD
.end
